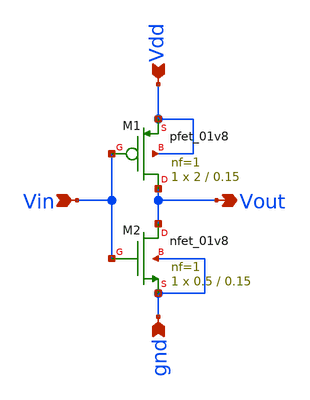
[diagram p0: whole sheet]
** sch_path: second_test/inv_vtc.sch
**.subckt inv_vtc Vin Vdd gnd Vout
*.ipin Vin
*.ipin Vdd
*.ipin gnd
*.opin Vout
XM1 Vout Vin Vdd Vdd sky130_fd_pr__pfet_01v8 L=0.15 W=2 nf=1 ad='int((nf+1)/2) * W/nf * 0.29' as='int((nf+2)/2) * W/nf * 0.29'
+ pd='2*int((nf+1)/2) * (W/nf + 0.29)' ps='2*int((nf+2)/2) * (W/nf + 0.29)' nrd='0.29 / W' nrs='0.29 / W'
+ sa=0 sb=0 sd=0 mult=1 m=1
XM2 Vout Vin gnd gnd sky130_fd_pr__nfet_01v8 L=0.15 W=0.5 nf=1 ad='int((nf+1)/2) * W/nf * 0.29' as='int((nf+2)/2) * W/nf * 0.29'
+ pd='2*int((nf+1)/2) * (W/nf + 0.29)' ps='2*int((nf+2)/2) * (W/nf + 0.29)' nrd='0.29 / W' nrs='0.29 / W'
+ sa=0 sb=0 sd=0 mult=1 m=1
**.ends
.end
